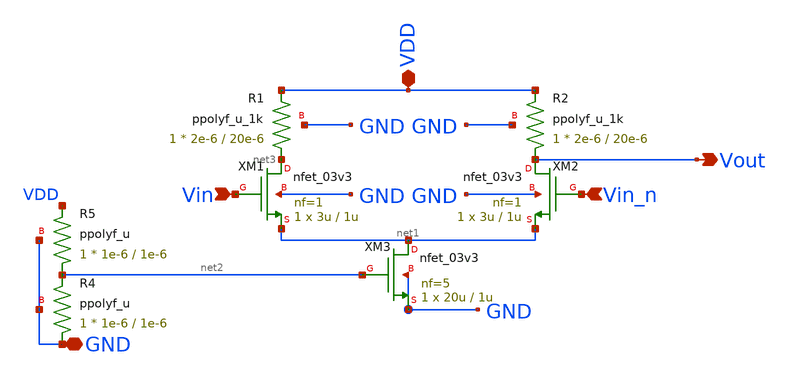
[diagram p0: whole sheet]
** sch_path: blocks/pll/diffpair.sch
**.subckt diffpair Vin Vin_n VDD Vout GND
*.ipin Vin
*.ipin Vin_n
*.iopin VDD
*.opin Vout
*.iopin GND
XM1 net3 Vin net1 GND nfet_03v3 L=1u W=3u nf=1 ad='int((nf+1)/2) * W/nf * 0.18u' as='int((nf+2)/2) * W/nf * 0.18u'
+ pd='2*int((nf+1)/2) * (W/nf + 0.18u)' ps='2*int((nf+2)/2) * (W/nf + 0.18u)' nrd='0.18u / W' nrs='0.18u / W'
+ sa=0 sb=0 sd=0 m=1
XM2 Vout Vin_n net1 GND nfet_03v3 L=1u W=3u nf=1 ad='int((nf+1)/2) * W/nf * 0.18u' as='int((nf+2)/2) * W/nf * 0.18u'
+ pd='2*int((nf+1)/2) * (W/nf + 0.18u)' ps='2*int((nf+2)/2) * (W/nf + 0.18u)' nrd='0.18u / W' nrs='0.18u / W'
+ sa=0 sb=0 sd=0 m=1
XM3 net1 net2 GND GND nfet_03v3 L=1u W=20u nf=5 ad='int((nf+1)/2) * W/nf * 0.18u' as='int((nf+2)/2) * W/nf * 0.18u'
+ pd='2*int((nf+1)/2) * (W/nf + 0.18u)' ps='2*int((nf+2)/2) * (W/nf + 0.18u)' nrd='0.18u / W' nrs='0.18u / W'
+ sa=0 sb=0 sd=0 m=1
XR1 net3 VDD GND ppolyf_u_1k r_width=2e-6 r_length=20e-6 m=1
XR2 Vout VDD GND ppolyf_u_1k r_width=2e-6 r_length=20e-6 m=1
XR4 GND net2 GND ppolyf_u r_width=1e-6 r_length=1e-6 m=1
XR5 net2 VDD GND ppolyf_u r_width=1e-6 r_length=1e-6 m=1
**.ends
.end
